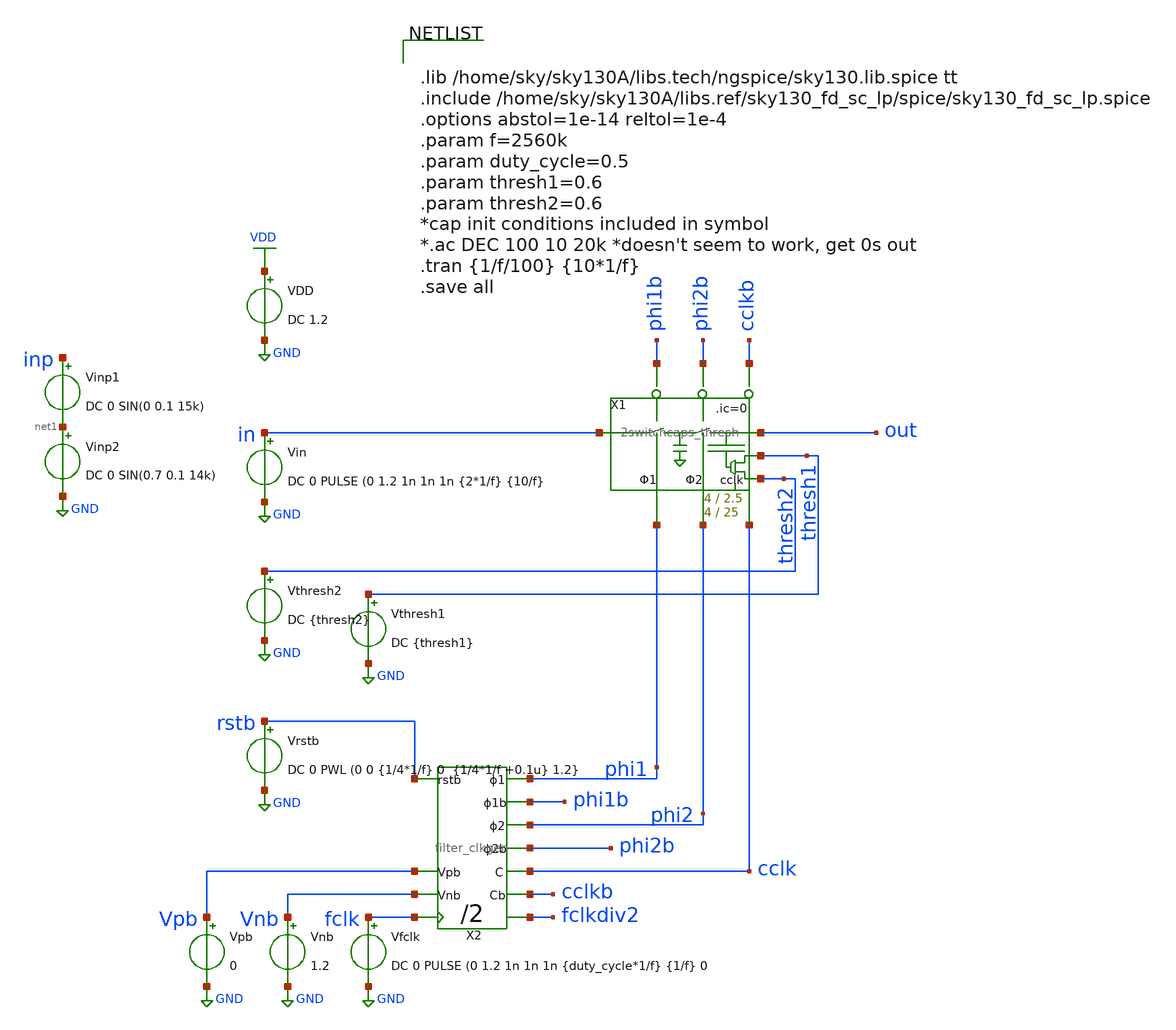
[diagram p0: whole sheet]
** sch_path: xschem/Switched_Caps/2switchcaps_thresh_tb.sch
**.subckt 2switchcaps_thresh_tb
Vin in GND DC 0 PULSE (0 1.2 1n 1n 1n {2*1/f} {10/f}
VDD VDD GND DC 1.2
Vfclk fclk GND DC 0 PULSE (0 1.2 1n 1n 1n {duty_cycle*1/f} {1/f} 0
X2 rstb fclk phi2b phi2 phi1b phi1 cclkb cclk fclkdiv2 Vpb Vnb filter_clkgen
Vthresh1 thresh1 GND DC {thresh1}
Vthresh2 thresh2 GND DC {thresh2}
Vrstb rstb GND DC 0 PWL (0 0 {1/4*1/f} 0 {1/4*1/f +0.1u} 1.2}
X1 in out phi2 phi1 phi1b phi2b thresh2 cclk thresh1 cclkb 2switchcaps_thresh Wcap1=4 Lcap1=2.5 Wcap2=4 Lcap2=25
Vpb Vpb GND 0
Vnb Vnb GND 1.2
Vinp1 inp net1 DC 0 SIN(0 0.1 15k)
Vinp2 net1 GND DC 0 SIN(0.7 0.1 14k)
**** begin user architecture code


.lib /home/sky/sky130A/libs.tech/ngspice/sky130.lib.spice tt
.include /home/sky/sky130A/libs.ref/sky130_fd_sc_lp/spice/sky130_fd_sc_lp.spice
.options abstol=1e-14 reltol=1e-4
.param f=2560k
.param duty_cycle=0.5
.param thresh1=0.6
.param thresh2=0.6
*cap init conditions included in symbol
*.ac DEC 100 10 20k *doesn't seem to work, get 0s out
.tran {1/f/100} {10*1/f}
.save all


**** end user architecture code
**.ends
.GLOBAL GND
.GLOBAL VDD
.end
